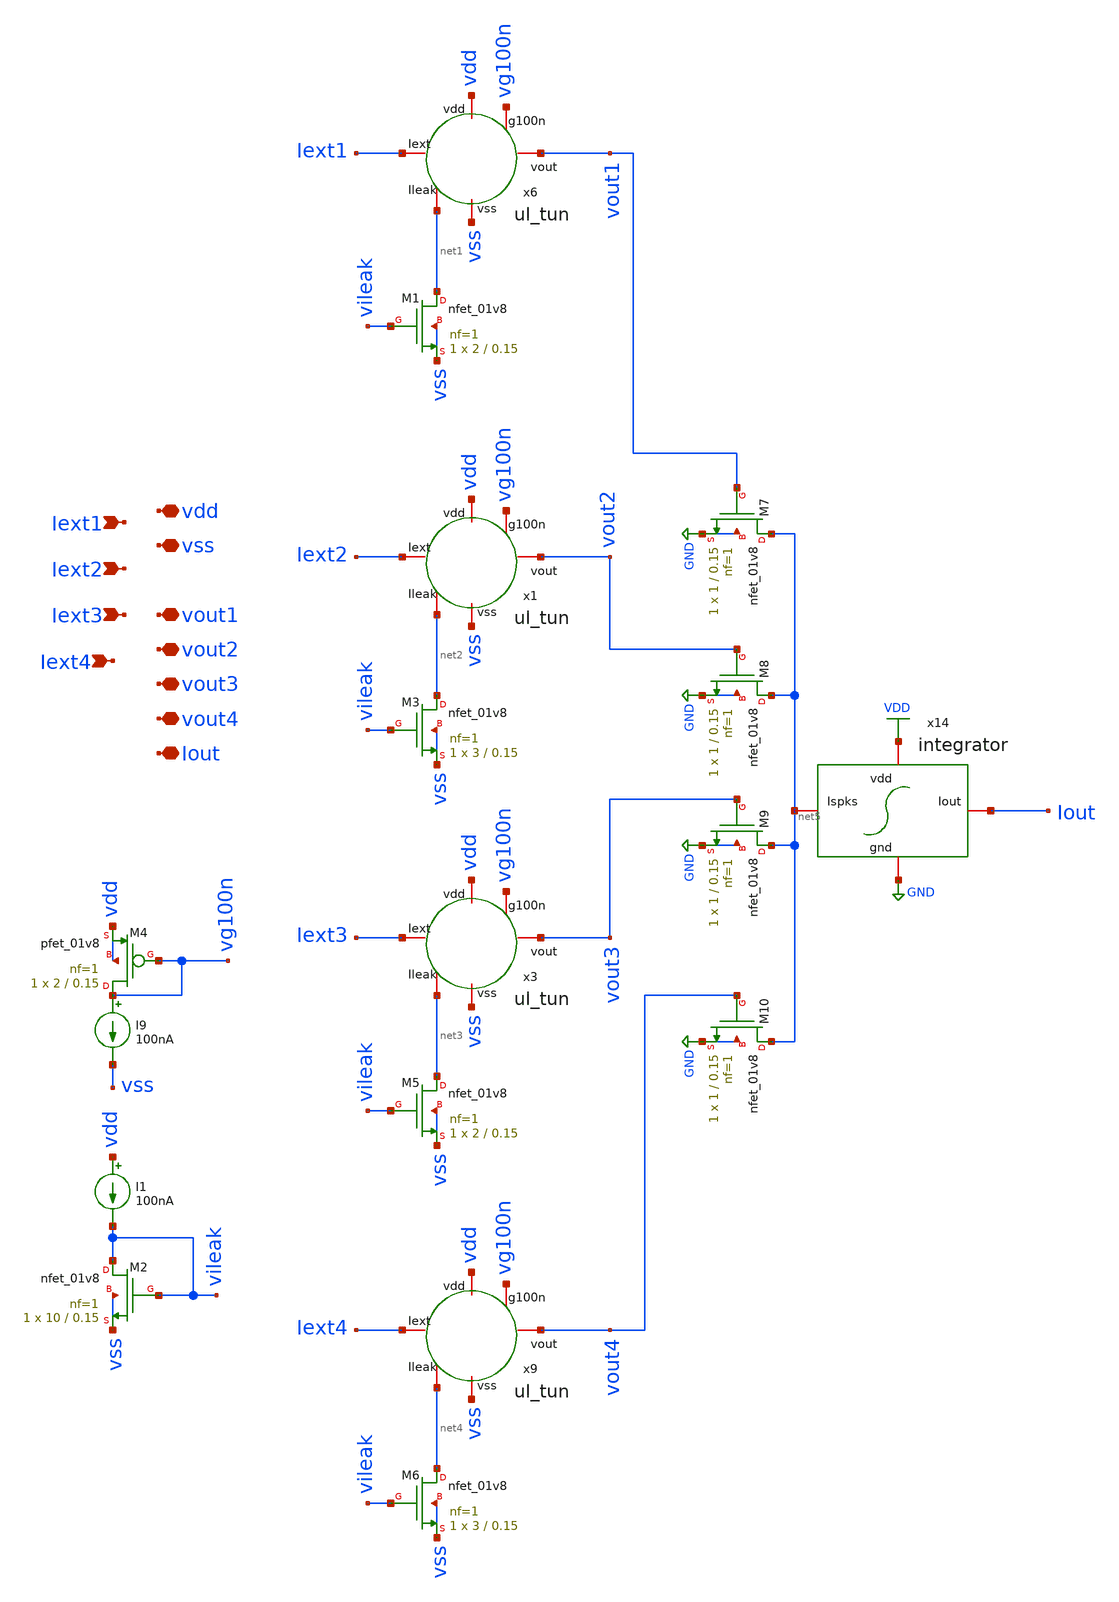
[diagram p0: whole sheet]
** sch_path: layer/layer_output.sch
**.subckt layer_output vdd vss Iext1 Iout Iext2 Iext3 Iext4 vout1 vout2 vout3 vout4
*.iopin vdd
*.iopin vss
*.ipin Iext1
*.iopin Iout
*.ipin Iext2
*.ipin Iext3
*.ipin Iext4
*.iopin vout1
*.iopin vout2
*.iopin vout3
*.iopin vout4
x6 Iext1 vdd vg100n vout1 net1 vss ul_tun
I9 vg100n vss 100nA
XM4 vg100n vg100n vdd vdd sky130_fd_pr__pfet_01v8 L=0.15 W=2 nf=1 ad='int((nf+1)/2) * W/nf * 0.29' as='int((nf+2)/2) * W/nf * 0.29'
+ pd='2*int((nf+1)/2) * (W/nf + 0.29)' ps='2*int((nf+2)/2) * (W/nf + 0.29)' nrd='0.29 / W' nrs='0.29 / W'
+ sa=0 sb=0 sd=0 mult=1 m=1
XM1 net1 vileak vss vss sky130_fd_pr__nfet_01v8 L=0.15 W=2 nf=1 ad='int((nf+1)/2) * W/nf * 0.29' as='int((nf+2)/2) * W/nf * 0.29'
+ pd='2*int((nf+1)/2) * (W/nf + 0.29)' ps='2*int((nf+2)/2) * (W/nf + 0.29)' nrd='0.29 / W' nrs='0.29 / W'
+ sa=0 sb=0 sd=0 mult=1 m=1
XM2 vileak vileak vss vss sky130_fd_pr__nfet_01v8 L=0.15 W=10 nf=1 ad='int((nf+1)/2) * W/nf * 0.29' as='int((nf+2)/2) * W/nf * 0.29'
+ pd='2*int((nf+1)/2) * (W/nf + 0.29)' ps='2*int((nf+2)/2) * (W/nf + 0.29)' nrd='0.29 / W' nrs='0.29 / W'
+ sa=0 sb=0 sd=0 mult=1 m=1
I1 vdd vileak 100nA
x1 Iext2 vdd vg100n vout2 net2 vss ul_tun
XM3 net2 vileak vss vss sky130_fd_pr__nfet_01v8 L=0.15 W=3 nf=1 ad='int((nf+1)/2) * W/nf * 0.29' as='int((nf+2)/2) * W/nf * 0.29'
+ pd='2*int((nf+1)/2) * (W/nf + 0.29)' ps='2*int((nf+2)/2) * (W/nf + 0.29)' nrd='0.29 / W' nrs='0.29 / W'
+ sa=0 sb=0 sd=0 mult=1 m=1
x3 Iext3 vdd vg100n vout3 net3 vss ul_tun
XM5 net3 vileak vss vss sky130_fd_pr__nfet_01v8 L=0.15 W=2 nf=1 ad='int((nf+1)/2) * W/nf * 0.29' as='int((nf+2)/2) * W/nf * 0.29'
+ pd='2*int((nf+1)/2) * (W/nf + 0.29)' ps='2*int((nf+2)/2) * (W/nf + 0.29)' nrd='0.29 / W' nrs='0.29 / W'
+ sa=0 sb=0 sd=0 mult=1 m=1
x9 Iext4 vdd vg100n vout4 net4 vss ul_tun
XM6 net4 vileak vss vss sky130_fd_pr__nfet_01v8 L=0.15 W=3 nf=1 ad='int((nf+1)/2) * W/nf * 0.29' as='int((nf+2)/2) * W/nf * 0.29'
+ pd='2*int((nf+1)/2) * (W/nf + 0.29)' ps='2*int((nf+2)/2) * (W/nf + 0.29)' nrd='0.29 / W' nrs='0.29 / W'
+ sa=0 sb=0 sd=0 mult=1 m=1
x14 VDD Iout net5 GND integrator
XM7 net5 vout1 GND GND sky130_fd_pr__nfet_01v8 L=0.15 W=1 nf=1 ad='int((nf+1)/2) * W/nf * 0.29' as='int((nf+2)/2) * W/nf * 0.29'
+ pd='2*int((nf+1)/2) * (W/nf + 0.29)' ps='2*int((nf+2)/2) * (W/nf + 0.29)' nrd='0.29 / W' nrs='0.29 / W'
+ sa=0 sb=0 sd=0 mult=1 m=1
XM8 net5 vout2 GND GND sky130_fd_pr__nfet_01v8 L=0.15 W=1 nf=1 ad='int((nf+1)/2) * W/nf * 0.29' as='int((nf+2)/2) * W/nf * 0.29'
+ pd='2*int((nf+1)/2) * (W/nf + 0.29)' ps='2*int((nf+2)/2) * (W/nf + 0.29)' nrd='0.29 / W' nrs='0.29 / W'
+ sa=0 sb=0 sd=0 mult=1 m=1
XM9 net5 vout3 GND GND sky130_fd_pr__nfet_01v8 L=0.15 W=1 nf=1 ad='int((nf+1)/2) * W/nf * 0.29' as='int((nf+2)/2) * W/nf * 0.29'
+ pd='2*int((nf+1)/2) * (W/nf + 0.29)' ps='2*int((nf+2)/2) * (W/nf + 0.29)' nrd='0.29 / W' nrs='0.29 / W'
+ sa=0 sb=0 sd=0 mult=1 m=1
XM10 net5 vout4 GND GND sky130_fd_pr__nfet_01v8 L=0.15 W=1 nf=1 ad='int((nf+1)/2) * W/nf * 0.29' as='int((nf+2)/2) * W/nf * 0.29'
+ pd='2*int((nf+1)/2) * (W/nf + 0.29)' ps='2*int((nf+2)/2) * (W/nf + 0.29)' nrd='0.29 / W' nrs='0.29 / W'
+ sa=0 sb=0 sd=0 mult=1 m=1
**.ends

* expanding   symbol:  Neuron/ultralif/ul_tun.sym # of pins=6
** sym_path: Neuron/ultralif/ul_tun.sym
** sch_path: Neuron/ultralif/ul_tun.sch
.subckt ul_tun Iext vdd g100n vout Ileak vss
*.iopin Iext
*.iopin vout
*.iopin vss
*.iopin Ileak
*.iopin vdd
*.iopin g100n
XM1 Ileak Ileak net1 vdd sky130_fd_pr__pfet_01v8 L=10 W=1 nf=1 ad='int((nf+1)/2) * W/nf * 0.29' as='int((nf+2)/2) * W/nf * 0.29'
+ pd='2*int((nf+1)/2) * (W/nf + 0.29)' ps='2*int((nf+2)/2) * (W/nf + 0.29)' nrd='0.29 / W' nrs='0.29 / W'
+ sa=0 sb=0 sd=0 mult=1 m=1
XM2 Ileak net2 net1 vdd sky130_fd_pr__pfet_01v8 L=0.15 W=1.5 nf=1 ad='int((nf+1)/2) * W/nf * 0.29' as='int((nf+2)/2) * W/nf * 0.29'
+ pd='2*int((nf+1)/2) * (W/nf + 0.29)' ps='2*int((nf+2)/2) * (W/nf + 0.29)' nrd='0.29 / W' nrs='0.29 / W'
+ sa=0 sb=0 sd=0 mult=1 m=1
XM3 net2 net2 net1 vdd sky130_fd_pr__pfet_01v8 L=0.15 W=15 nf=1 ad='int((nf+1)/2) * W/nf * 0.29' as='int((nf+2)/2) * W/nf * 0.29'
+ pd='2*int((nf+1)/2) * (W/nf + 0.29)' ps='2*int((nf+2)/2) * (W/nf + 0.29)' nrd='0.29 / W' nrs='0.29 / W'
+ sa=0 sb=0 sd=0 mult=1 m=1
XM4 net2 Ileak vss vss sky130_fd_pr__nfet_01v8 L=4 W=1 nf=1 ad='int((1 + 1)/2) * 1 / 1 * 0.29' as='int((1 + 2)/2) * 1 / 1 * 0.29'
+ pd='2*int((1 + 1)/2) * (1 / 1 + 0.29)' ps='2*int((1 + 2)/2) * (1 / 1 + 0.29)' nrd='0.29 / 1 ' nrs='0.29 / 1 '
+ sa=0 sb=0 sd=0 mult=1 m=1
C1 net1 vss 1p m=1
XM5 vout_n Ileak vss vss sky130_fd_pr__nfet_01v8 L=0.15 W=1 nf=1 ad='int((1 + 1)/2) * 1 / 1 * 0.29' as='int((1 + 2)/2) * 1 / 1 * 0.29'
+ pd='2*int((1 + 1)/2) * (1 / 1 + 0.29)' ps='2*int((1 + 2)/2) * (1 / 1 + 0.29)' nrd='0.29 / 1 ' nrs='0.29 / 1 '
+ sa=0 sb=0 sd=0 mult=1 m=1
XM6 vout_n g100n vdd vdd sky130_fd_pr__pfet_01v8 L=0.15 W=2 nf=1 ad='int((nf+1)/2) * W/nf * 0.29' as='int((nf+2)/2) * W/nf * 0.29'
+ pd='2*int((nf+1)/2) * (W/nf + 0.29)' ps='2*int((nf+2)/2) * (W/nf + 0.29)' nrd='0.29 / W' nrs='0.29 / W'
+ sa=0 sb=0 sd=0 mult=1 m=1
XM7 vout vout_n vss vss sky130_fd_pr__nfet_01v8 L=0.15 W=1 nf=1 ad='int((1 + 1)/2) * 1 / 1 * 0.29' as='int((1 + 2)/2) * 1 / 1 * 0.29'
+ pd='2*int((1 + 1)/2) * (1 / 1 + 0.29)' ps='2*int((1 + 2)/2) * (1 / 1 + 0.29)' nrd='0.29 / 1 ' nrs='0.29 / 1 '
+ sa=0 sb=0 sd=0 mult=1 m=1
XM8 vout vout_n vdd vdd sky130_fd_pr__pfet_01v8 L=0.15 W=2 nf=1 ad='int((nf+1)/2) * W/nf * 0.29' as='int((nf+2)/2) * W/nf * 0.29'
+ pd='2*int((nf+1)/2) * (W/nf + 0.29)' ps='2*int((nf+2)/2) * (W/nf + 0.29)' nrd='0.29 / W' nrs='0.29 / W'
+ sa=0 sb=0 sd=0 mult=1 m=1
XM9 net1 vout Iext vdd sky130_fd_pr__pfet_01v8 L=0.15 W=2 nf=1 ad='int((nf+1)/2) * W/nf * 0.29' as='int((nf+2)/2) * W/nf * 0.29'
+ pd='2*int((nf+1)/2) * (W/nf + 0.29)' ps='2*int((nf+2)/2) * (W/nf + 0.29)' nrd='0.29 / W' nrs='0.29 / W'
+ sa=0 sb=0 sd=0 mult=1 m=1
.ends


* expanding   symbol:  Neuron/ultralif/integrator.sym # of pins=4
** sym_path: Neuron/ultralif/integrator.sym
** sch_path: Neuron/ultralif/integrator.sch
.subckt integrator vdd Iout Ispks gnd
*.iopin Ispks
*.iopin Iout
*.iopin vdd
*.iopin gnd
XMIn Ispks vx vsyn vdd sky130_fd_pr__pfet_01v8 L=0.15 W=5 nf=1 ad='int((nf+1)/2) * W/nf * 0.29' as='int((nf+2)/2) * W/nf * 0.29'
+ pd='2*int((nf+1)/2) * (W/nf + 0.29)' ps='2*int((nf+2)/2) * (W/nf + 0.29)' nrd='0.29 / W' nrs='0.29 / W'
+ sa=0 sb=0 sd=0 mult=1 m=1
XM3 vsyn vdd vdd vdd sky130_fd_pr__pfet_01v8 L=0.15 W=5 nf=1 ad='int((nf+1)/2) * W/nf * 0.29' as='int((nf+2)/2) * W/nf * 0.29'
+ pd='2*int((nf+1)/2) * (W/nf + 0.29)' ps='2*int((nf+2)/2) * (W/nf + 0.29)' nrd='0.29 / W' nrs='0.29 / W'
+ sa=0 sb=0 sd=0 mult=1 m=1
XM4 Iout vsyn vdd vdd sky130_fd_pr__pfet_01v8 L=0.15 W=24.5 nf=1 ad='int((nf+1)/2) * W/nf * 0.29' as='int((nf+2)/2) * W/nf * 0.29'
+ pd='2*int((nf+1)/2) * (W/nf + 0.29)' ps='2*int((nf+2)/2) * (W/nf + 0.29)' nrd='0.29 / W' nrs='0.29 / W'
+ sa=0 sb=0 sd=0 mult=1 m=1
XCsyn vdd vsyn sky130_fd_pr__cap_mim_m3_1 W=22.5 L=22 MF=1 m=1
XR2 vx vdd sky130_fd_pr__res_generic_po W=1 L=1 m=1
XR1 gnd vx sky130_fd_pr__res_generic_po W=1 L=1 m=1
.ends

.GLOBAL GND
.GLOBAL VDD
.end
